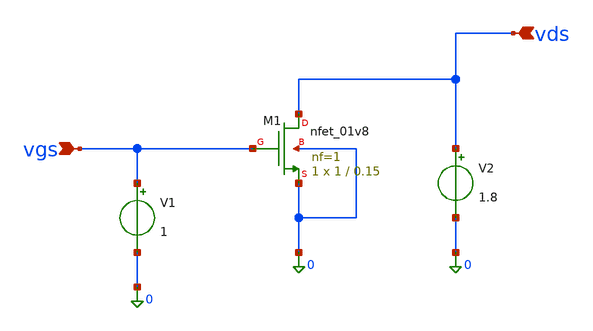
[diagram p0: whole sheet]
** sch_path: nmos.sch
**.subckt nmos vgs vds
*.ipin vgs
*.ipin vds
XM1 vds vgs 0 0 sky130_fd_pr__nfet_01v8 L=0.15 W=1 nf=1 ad='int((1 + 1)/2) * 1 / 1 * 0.29' as='int((1 + 2)/2) * 1 / 1 * 0.29'
+ pd='2*int((1 + 1)/2) * (1 / 1 + 0.29)' ps='2*int((1 + 2)/2) * (1 / 1 + 0.29)' nrd='0.29 / 1 ' nrs='0.29 / 1 '
+ sa=0 sb=0 sd=0 mult=1 m=1
V1 vgs 0 1
V2 vds 0 1.8
**** begin user architecture code


.lib /foss/pdks/ciel/sky130/versions/7b70722e33c03fcb5dabcf4d479fb0822d9251c9/sky130A/libs.tech/ngspice/sky130.lib.spice tt
.control
  save all
  save @m.xm1.msky130_fd_pr__nfet_01v8[id]
   save @m.xm1.msky130_fd_pr__nfet_01v8[gm]

  op
dc v2 0 1.8 0.1 v1 0 1.8 0.6
  plot @m.xm1.msky130_fd_pr__nfet_01v8[id]
  plot @m.xm1.msky130_fd_pr__nfet_01v8[gm]


   dc v1 0 1.8 0.1
  plot @m.xm1.msky130_fd_pr__nfet_01v8[id]
  plot @m.xm1.msky130_fd_pr__nfet_01v8[gm]

  print @m.xm1.msky130_fd_pr__nfet_01v8[id]
  print @m.xm1.msky130_fd_pr__nfet_01v8[gm]
  print @m.xm1.msky130_fd_pr__nfet_01v8[vth]
  print @m.xm1.msky130_fd_pr__nfet_01v8[vgs]
  print @m.xm1.msky130_fd_pr__nfet_01v8[vdsat]
  print @m.xm1.msky130_fd_pr__nfet_01v8[vds]
  print @m.xm1.msky130_fd_pr__nfet_01v8[gds]


  write moschar.raw
.endc


**** end user architecture code
**.ends
.end
